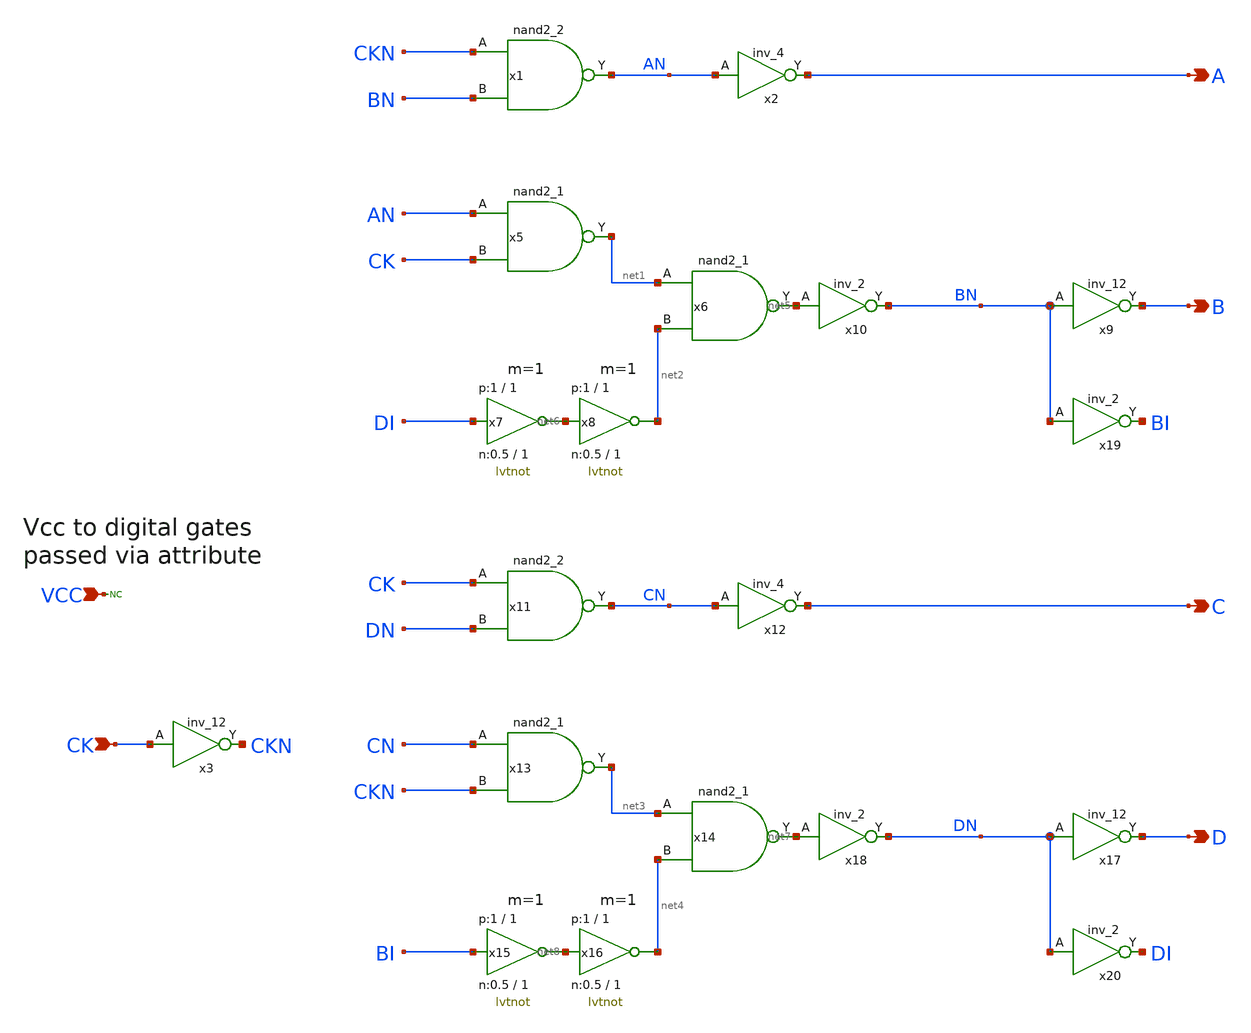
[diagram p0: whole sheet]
** sch_path: sky130_tests/charge_pump_phasegen.sch
* Copyright 2021 Stefan Frederik Schippers
* Licensed under the Apache License, Version 2.0 (the "License");
* you may not use this file except in compliance with the License.
* You may obtain a copy of the License at
* https://www.apache.org/licenses/LICENSE-2.0
* Unless required by applicable law or agreed to in writing, software
* distributed under the License is distributed on an "AS IS" BASIS,
* WITHOUT WARRANTIES OR CONDITIONS OF ANY KIND, either express or implied.
* See the License for the specific language governing permissions and
* limitations under the License.
**.subckt charge_pump_phasegen CK A B C D VCC
*.ipin CK
*.opin A
*.opin B
*.opin C
*.opin D
*.ipin VCC
x1 CKN BN GND GND VCC VCC AN sky130_fd_sc_hd__nand2_2
x2 AN GND GND VCC VCC A sky130_fd_sc_hd__inv_4
x5 AN CK GND GND VCC VCC net1 sky130_fd_sc_hd__nand2_1
x6 net1 net2 GND GND VCC VCC net5 sky130_fd_sc_hd__nand2_1
x7 net6 DI VCC GND lvtnot W_N=0.5 L_N=1 W_P=1 L_P=1 m=1
x8 net2 net6 VCC GND lvtnot W_N=0.5 L_N=1 W_P=1 L_P=1 m=1
x9 BN GND GND VCC VCC B sky130_fd_sc_hd__inv_12
x10 net5 GND GND VCC VCC BN sky130_fd_sc_hd__inv_2
x11 CK DN GND GND VCC VCC CN sky130_fd_sc_hd__nand2_2
x12 CN GND GND VCC VCC C sky130_fd_sc_hd__inv_4
x13 CN CKN GND GND VCC VCC net3 sky130_fd_sc_hd__nand2_1
x14 net3 net4 GND GND VCC VCC net7 sky130_fd_sc_hd__nand2_1
x15 net8 BI VCC GND lvtnot W_N=0.5 L_N=1 W_P=1 L_P=1 m=1
x16 net4 net8 VCC GND lvtnot W_N=0.5 L_N=1 W_P=1 L_P=1 m=1
x17 DN GND GND VCC VCC D sky130_fd_sc_hd__inv_12
x18 net7 GND GND VCC VCC DN sky130_fd_sc_hd__inv_2
x3 CK GND GND VCC VCC CKN sky130_fd_sc_hd__inv_12
* noconn VCC
x19 BN GND GND VCC VCC BI sky130_fd_sc_hd__inv_2
x20 DN GND GND VCC VCC DI sky130_fd_sc_hd__inv_2
**.ends
.end
